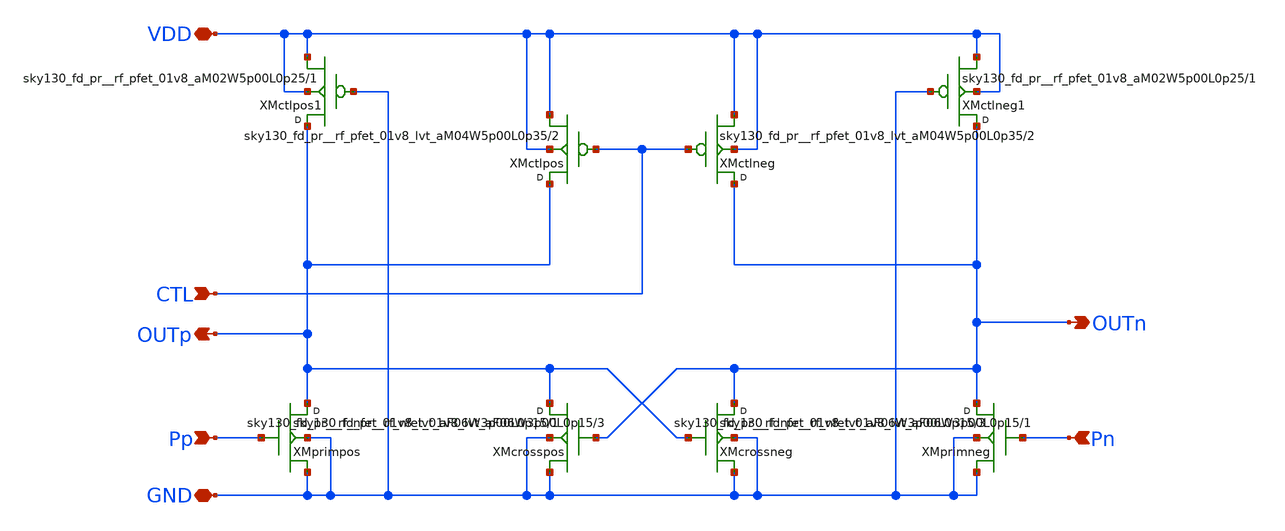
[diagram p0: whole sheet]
** sch_path: design/vco_2-4GHz_delaycell/vco_2-4GHz_delaycell_old.sch
**.subckt vco_2-4GHz_delaycell_old Pp Pn OUTn OUTp VDD GND CTL
*.ipin Pp
*.ipin Pn
*.opin OUTn
*.opin OUTp
*.iopin VDD
*.iopin GND
*.ipin CTL
XXMprimpos OUTp Pp GND GND sky130_fd_pr__rf_nfet_01v8_lvt_aF06W3p00L0p15 m=3
XXMcrossneg OUTn OUTp GND GND sky130_fd_pr__rf_nfet_01v8_lvt_aF06W3p00L0p15 m=1
XXMctlneg OUTn CTL VDD VDD sky130_fd_pr__rf_pfet_01v8_lvt_aM04W5p00L0p35 m=2
XXMctlpos OUTp CTL VDD VDD sky130_fd_pr__rf_pfet_01v8_lvt_aM04W5p00L0p35 m=2
XXMcrosspos OUTp OUTn GND GND sky130_fd_pr__rf_nfet_01v8_lvt_aF06W3p00L0p15 m=1
XXMprimneg OUTn Pn GND GND sky130_fd_pr__rf_nfet_01v8_lvt_aF06W3p00L0p15 m=3
XXMctlpos1 OUTp GND VDD VDD sky130_fd_pr__rf_pfet_01v8_aM02W5p00L0p25 m=1
XXMctlneg1 OUTn GND VDD VDD sky130_fd_pr__rf_pfet_01v8_aM02W5p00L0p25 m=1
**.ends
.end
